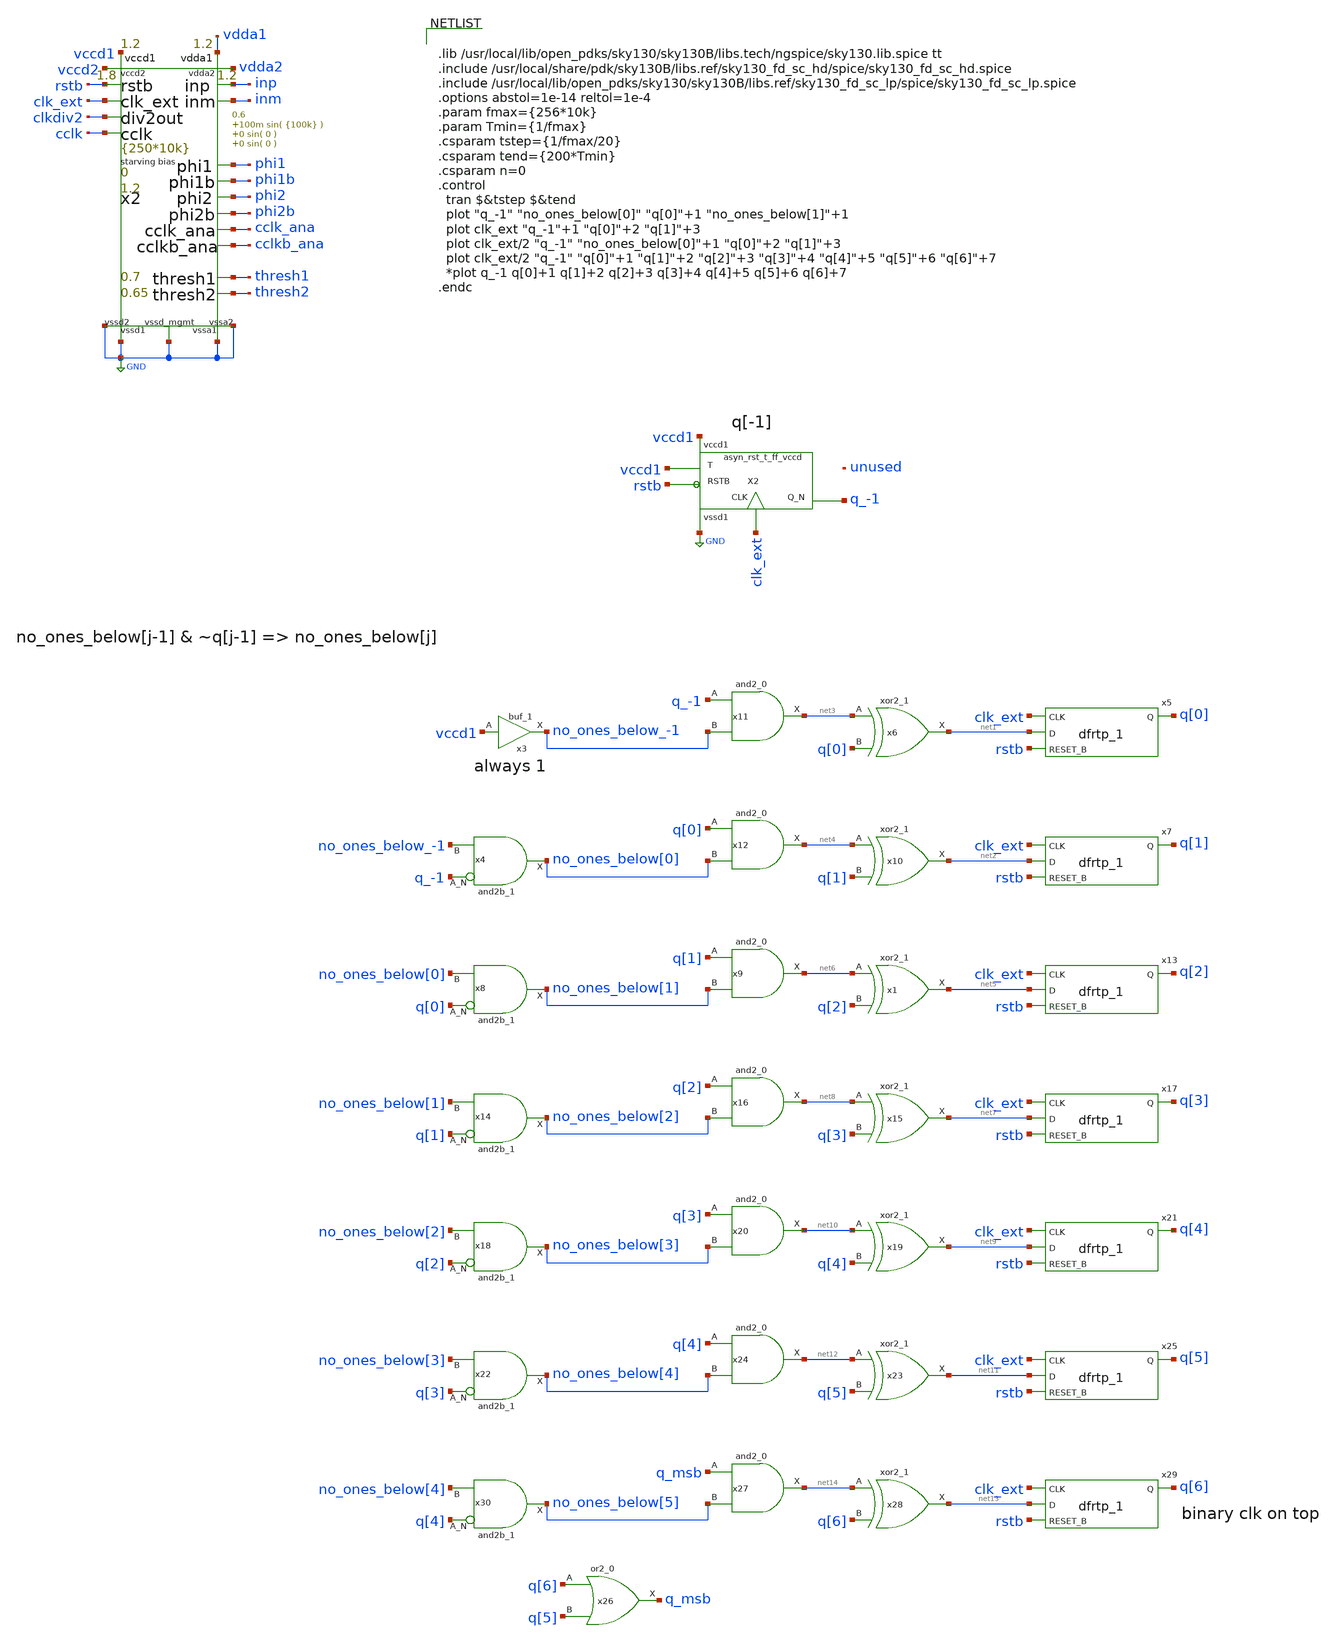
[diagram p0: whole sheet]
** sch_path: xschem/test_bench/gray_counter_tb.sch
**.subckt gray_counter_tb
x2 thresh1 thresh2 inp inm clk_ext rstb phi1 phi1 phi1b phi1b phi2 phi2 phi2b phi2b cclk_ana cclk_ana
+ cclkb_ana cclkb_ana clkdiv2 clkdiv2 cclk cclk vdda1 vccd1 vccd2 vdda2 GND GND GND GND GND risc_signals
+ p_vdda1=1.2 p_vdda2=1.2 p_vccd1=1.2 p_vccd2=1.8 p_vccd_mgmt=1.8 p_fclk={250*10k} p_duty_cycle=0.5 p_rstb_delay={1.5/p_fclk}
+ p_rstb_tr=5n p_thresh1=0.7 p_thresh2=0.65 p_vpb=0 p_vnb=1.2 p_vcm=0.6 p_amp1=100m p_f1={100k} p_amp2=0
+ p_f2=0 p_amp3=0 p_f3=0
x3 vccd1 gnd gnd vccd1 vccd1 no_ones_below_-1 sky130_fd_sc_hd__buf_1
x4 q_-1 no_ones_below_-1 gnd gnd vccd1 vccd1 no_ones_below[0] sky130_fd_sc_hd__and2b_1
x6 net3 q[0] gnd gnd vccd1 vccd1 net1 sky130_fd_sc_hd__xor2_1
x10 net4 q[1] gnd gnd vccd1 vccd1 net2 sky130_fd_sc_hd__xor2_1
x8 q[0] no_ones_below[0] gnd gnd vccd1 vccd1 no_ones_below[1] sky130_fd_sc_hd__and2b_1
X2 vccd1 clk_ext rstb q_-1 vccd1 GND asyn_rst_t_ff_vccd
x11 q_-1 no_ones_below_-1 gnd gnd vccd1 vccd1 net3 sky130_fd_sc_hd__and2_0
x12 q[0] no_ones_below[0] gnd gnd vccd1 vccd1 net4 sky130_fd_sc_hd__and2_0
x5 clk_ext net1 rstb gnd gnd vccd1 vccd1 q[0] sky130_fd_sc_hd__dfrtp_1
x7 clk_ext net2 rstb gnd gnd vccd1 vccd1 q[1] sky130_fd_sc_hd__dfrtp_1
x1 net6 q[2] gnd gnd vccd1 vccd1 net5 sky130_fd_sc_hd__xor2_1
x9 q[1] no_ones_below[1] gnd gnd vccd1 vccd1 net6 sky130_fd_sc_hd__and2_0
x13 clk_ext net5 rstb gnd gnd vccd1 vccd1 q[2] sky130_fd_sc_hd__dfrtp_1
x15 net8 q[3] gnd gnd vccd1 vccd1 net7 sky130_fd_sc_hd__xor2_1
x16 q[2] no_ones_below[2] gnd gnd vccd1 vccd1 net8 sky130_fd_sc_hd__and2_0
x17 clk_ext net7 rstb gnd gnd vccd1 vccd1 q[3] sky130_fd_sc_hd__dfrtp_1
x19 net10 q[4] gnd gnd vccd1 vccd1 net9 sky130_fd_sc_hd__xor2_1
x20 q[3] no_ones_below[3] gnd gnd vccd1 vccd1 net10 sky130_fd_sc_hd__and2_0
x21 clk_ext net9 rstb gnd gnd vccd1 vccd1 q[4] sky130_fd_sc_hd__dfrtp_1
x23 net12 q[5] gnd gnd vccd1 vccd1 net11 sky130_fd_sc_hd__xor2_1
x24 q[4] no_ones_below[4] gnd gnd vccd1 vccd1 net12 sky130_fd_sc_hd__and2_0
x25 clk_ext net11 rstb gnd gnd vccd1 vccd1 q[5] sky130_fd_sc_hd__dfrtp_1
x14 q[1] no_ones_below[1] gnd gnd vccd1 vccd1 no_ones_below[2] sky130_fd_sc_hd__and2b_1
x18 q[2] no_ones_below[2] gnd gnd vccd1 vccd1 no_ones_below[3] sky130_fd_sc_hd__and2b_1
x22 q[3] no_ones_below[3] gnd gnd vccd1 vccd1 no_ones_below[4] sky130_fd_sc_hd__and2b_1
x26 q[6] q[5] gnd gnd vccd1 vccd1 q_msb sky130_fd_sc_hd__or2_0
x27 q_msb no_ones_below[5] gnd gnd vccd1 vccd1 net14 sky130_fd_sc_hd__and2_0
x28 net14 q[6] gnd gnd vccd1 vccd1 net13 sky130_fd_sc_hd__xor2_1
x29 clk_ext net13 rstb gnd gnd vccd1 vccd1 q[6] sky130_fd_sc_hd__dfrtp_1
x30 q[4] no_ones_below[4] gnd gnd vccd1 vccd1 no_ones_below[5] sky130_fd_sc_hd__and2b_1
**** begin user architecture code


.lib /usr/local/lib/open_pdks/sky130/sky130B/libs.tech/ngspice/sky130.lib.spice tt
.include /usr/local/share/pdk/sky130B/libs.ref/sky130_fd_sc_hd/spice/sky130_fd_sc_hd.spice
.include /usr/local/lib/open_pdks/sky130/sky130B/libs.ref/sky130_fd_sc_lp/spice/sky130_fd_sc_lp.spice
.options abstol=1e-14 reltol=1e-4
.param fmax={256*10k}
.param Tmin={1/fmax}
.csparam tstep={1/fmax/20}
.csparam tend={200*Tmin}
.csparam n=0
.control
  tran $&tstep $&tend
  plot "q_-1" "no_ones_below[0]" "q[0]"+1 "no_ones_below[1]"+1
  plot clk_ext "q_-1"+1 "q[0]"+2 "q[1]"+3
  plot clk_ext/2 "q_-1" "no_ones_below[0]"+1 "q[0]"+2 "q[1]"+3
  plot clk_ext/2 "q_-1" "q[0]"+1 "q[1]"+2 "q[2]"+3 "q[3]"+4 "q[4]"+5 "q[5]"+6 "q[6]"+7
  *plot q_-1 q[0]+1 q[1]+2 q[2]+3 q[3]+4 q[4]+5 q[5]+6 q[6]+7
.endc


**** end user architecture code
**.ends
.GLOBAL GND
.end
